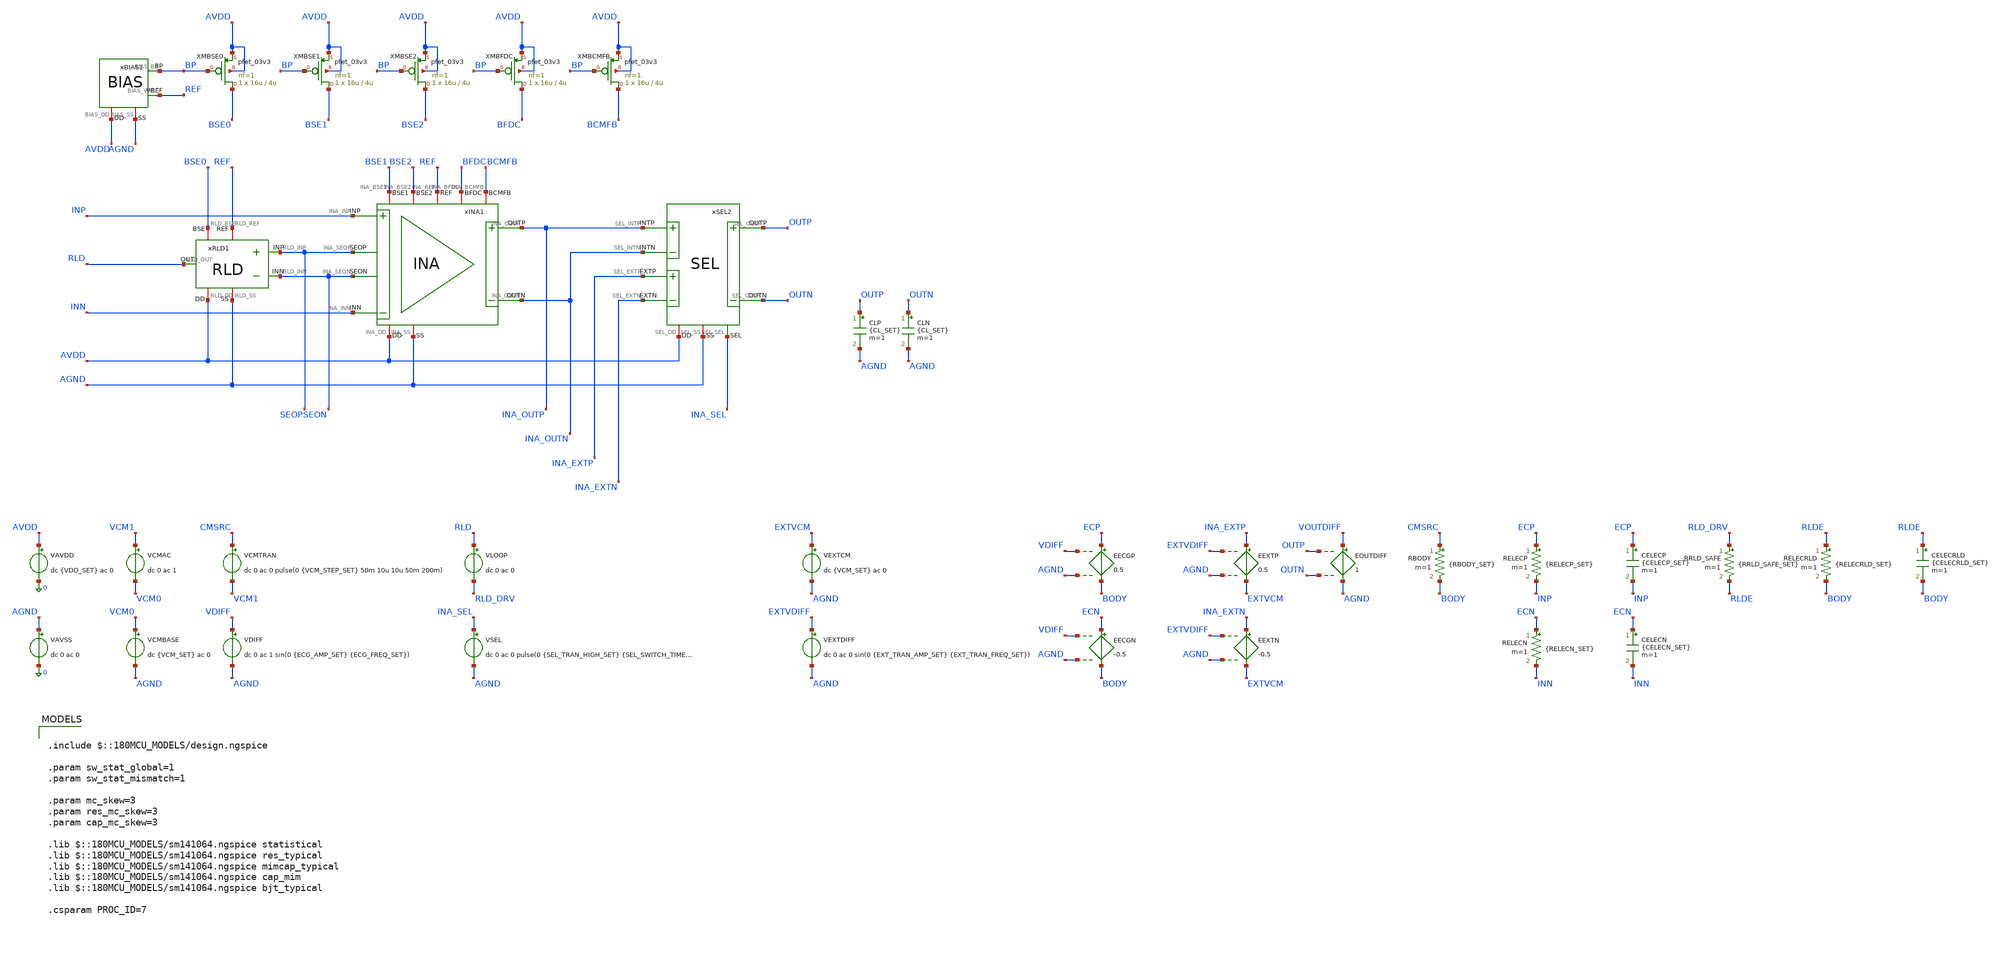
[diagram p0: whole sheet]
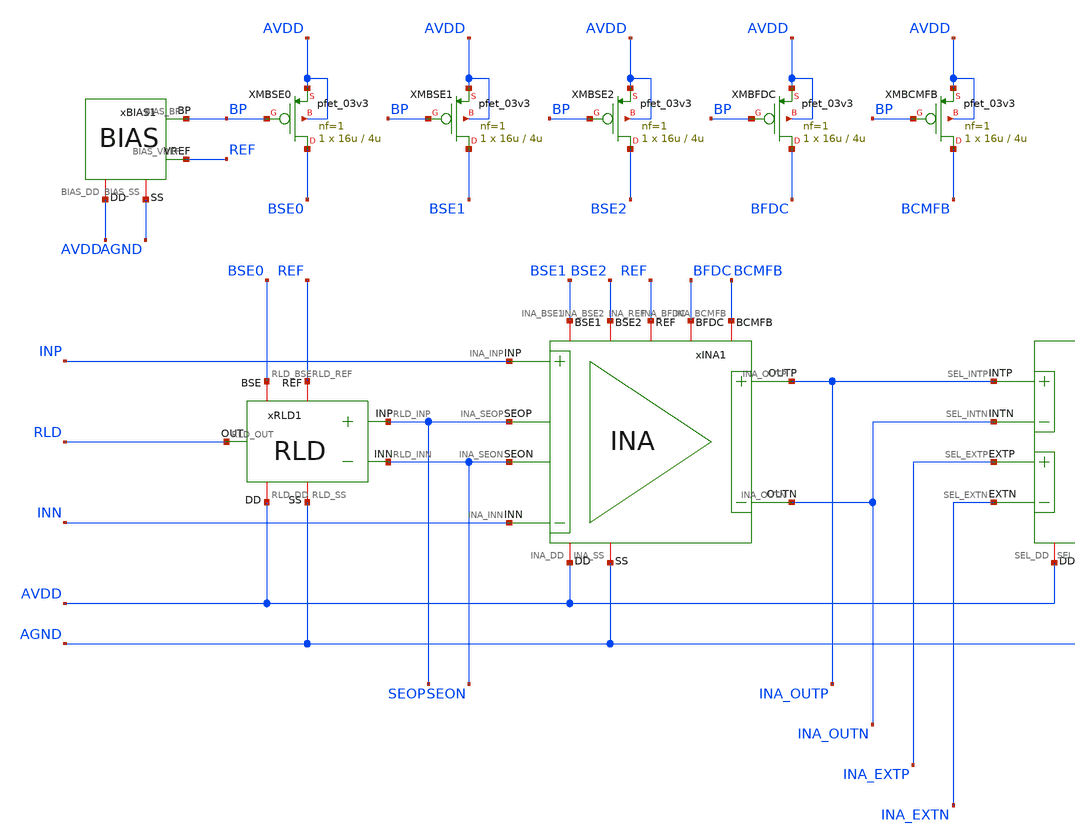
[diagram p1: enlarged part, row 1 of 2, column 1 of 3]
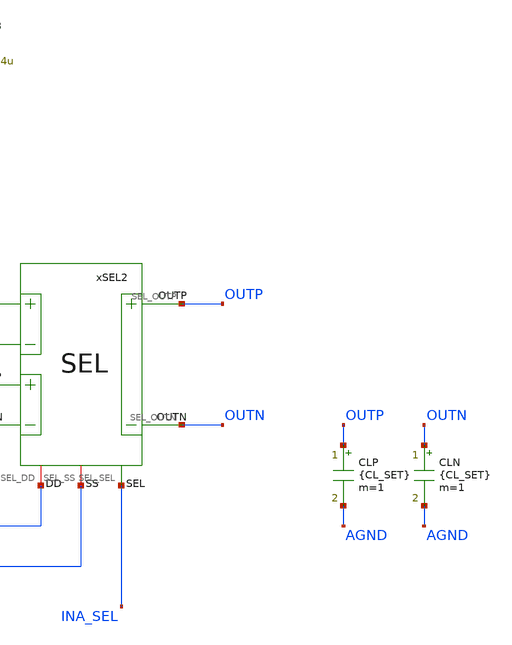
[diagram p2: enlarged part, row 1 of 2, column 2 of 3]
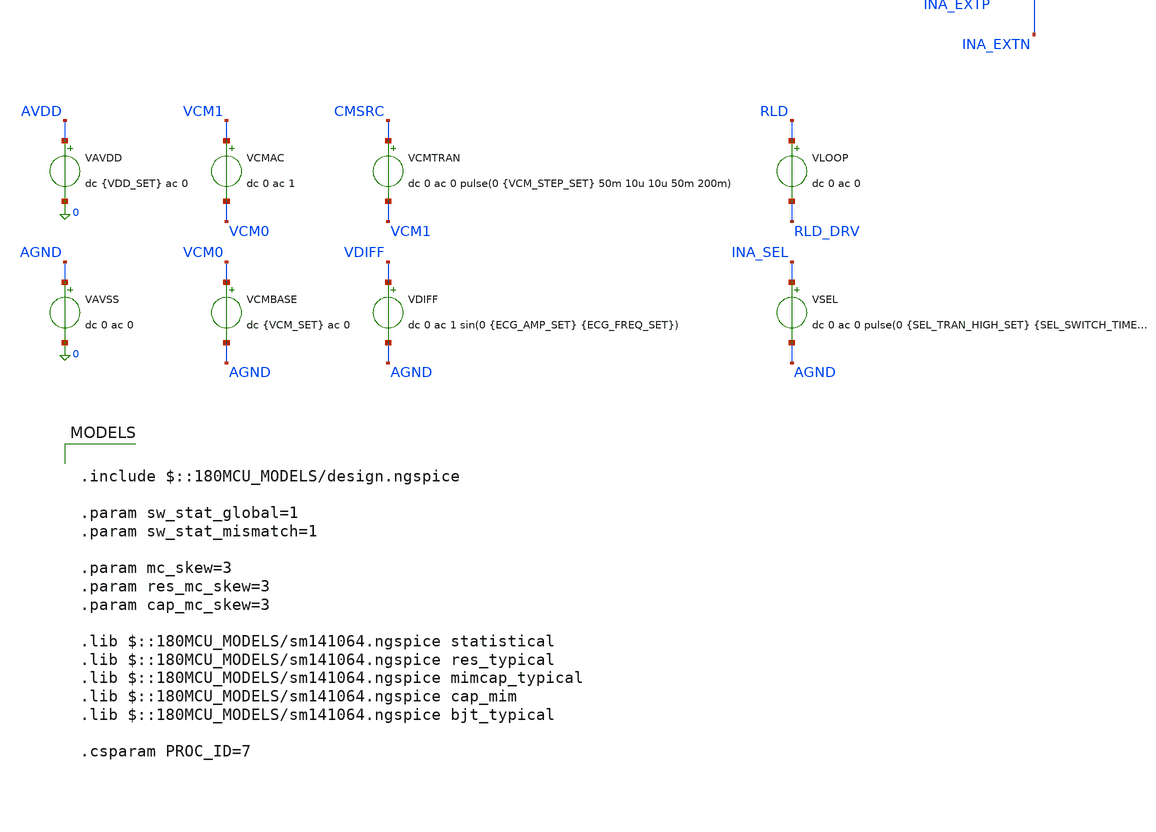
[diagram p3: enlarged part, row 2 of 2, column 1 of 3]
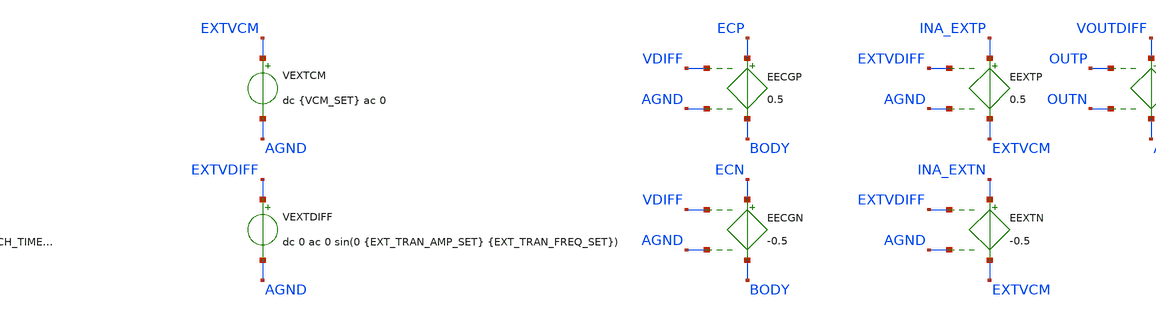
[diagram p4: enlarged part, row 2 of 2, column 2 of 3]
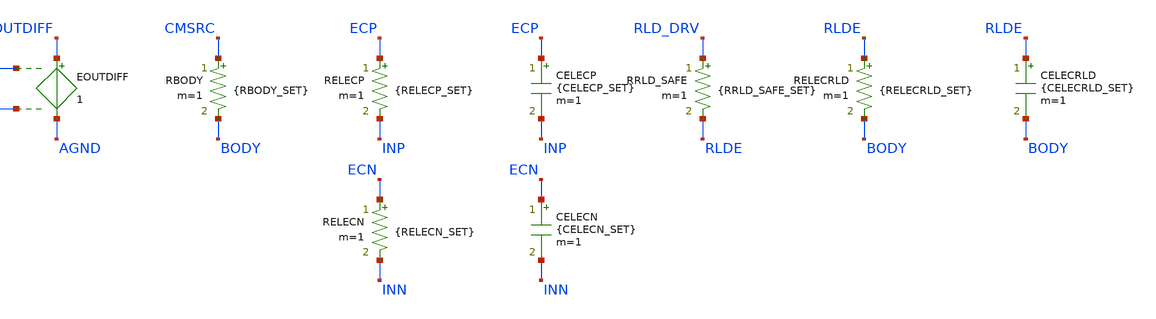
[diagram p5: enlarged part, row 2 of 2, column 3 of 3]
** sch_path: Design_Files/IC Design/Testbench/INA_RLD/INA_RLD_TB_FULL.sch
**.subckt INA_RLD_TB_FULL
xSEL2 AVDD AGND INA_OUTP INA_OUTN OUTN OUTP INA_EXTP INA_EXTN INA_SEL SEL
xINA1 AVDD AGND INP INN INA_OUTN BFDC INA_OUTP BCMFB REF SEON SEOP BSE1 BSE2 INA
xRLD1 AVDD AGND SEOP SEON RLD REF BSE0 RLD
CLP OUTP AGND {CL_SET} m=1
CLN OUTN AGND {CL_SET} m=1
xBIAS1 AVDD AGND BP REF BIAS
XMBSE0 BSE0 BP AVDD AVDD pfet_03v3 L=4u W=16u nf=1 ad='int((nf+1)/2) * W/nf * 0.18u' as='int((nf+2)/2) * W/nf * 0.18u'
+ pd='2*int((nf+1)/2) * (W/nf + 0.18u)' ps='2*int((nf+2)/2) * (W/nf + 0.18u)' nrd='0.18u / W' nrs='0.18u / W'
+ sa=0 sb=0 sd=0 m=1
XMBSE1 BSE1 BP AVDD AVDD pfet_03v3 L=4u W=16u nf=1 ad='int((nf+1)/2) * W/nf * 0.18u' as='int((nf+2)/2) * W/nf * 0.18u'
+ pd='2*int((nf+1)/2) * (W/nf + 0.18u)' ps='2*int((nf+2)/2) * (W/nf + 0.18u)' nrd='0.18u / W' nrs='0.18u / W'
+ sa=0 sb=0 sd=0 m=1
XMBSE2 BSE2 BP AVDD AVDD pfet_03v3 L=4u W=16u nf=1 ad='int((nf+1)/2) * W/nf * 0.18u' as='int((nf+2)/2) * W/nf * 0.18u'
+ pd='2*int((nf+1)/2) * (W/nf + 0.18u)' ps='2*int((nf+2)/2) * (W/nf + 0.18u)' nrd='0.18u / W' nrs='0.18u / W'
+ sa=0 sb=0 sd=0 m=1
XMBFDC BFDC BP AVDD AVDD pfet_03v3 L=4u W=16u nf=1 ad='int((nf+1)/2) * W/nf * 0.18u' as='int((nf+2)/2) * W/nf * 0.18u'
+ pd='2*int((nf+1)/2) * (W/nf + 0.18u)' ps='2*int((nf+2)/2) * (W/nf + 0.18u)' nrd='0.18u / W' nrs='0.18u / W'
+ sa=0 sb=0 sd=0 m=1
XMBCMFB BCMFB BP AVDD AVDD pfet_03v3 L=4u W=16u nf=1 ad='int((nf+1)/2) * W/nf * 0.18u' as='int((nf+2)/2) * W/nf * 0.18u'
+ pd='2*int((nf+1)/2) * (W/nf + 0.18u)' ps='2*int((nf+2)/2) * (W/nf + 0.18u)' nrd='0.18u / W' nrs='0.18u / W'
+ sa=0 sb=0 sd=0 m=1
VAVDD AVDD 0 dc {VDD_SET} ac 0
.save i(vavdd)
VCMBASE VCM0 AGND dc {VCM_SET} ac 0
VCMAC VCM1 VCM0 dc 0 ac 1
VAVSS AGND 0 dc 0 ac 0
VCMTRAN CMSRC VCM1 dc 0 ac 0 pulse(0 {VCM_STEP_SET} 50m 10u 10u 50m 200m)
EECGP ECP BODY VDIFF AGND 0.5
EECGN ECN BODY VDIFF AGND -0.5
EEXTP INA_EXTP EXTVCM EXTVDIFF AGND 0.5
VDIFF VDIFF AGND dc 0 ac 1 sin(0 {ECG_AMP_SET} {ECG_FREQ_SET})
VLOOP RLD RLD_DRV dc 0 ac 0
.save i(vloop)
VSEL INA_SEL AGND dc 0 ac 0 pulse(0 {SEL_TRAN_HIGH_SET} {SEL_SWITCH_TIME_SET} 1u 1u 400m 800m)
VEXTCM EXTVCM AGND dc {VCM_SET} ac 0
VEXTDIFF EXTVDIFF AGND dc 0 ac 0 sin(0 {EXT_TRAN_AMP_SET} {EXT_TRAN_FREQ_SET})
EEXTN INA_EXTN EXTVCM EXTVDIFF AGND -0.5
EOUTDIFF VOUTDIFF AGND OUTP OUTN 1
RBODY CMSRC BODY {RBODY_SET} m=1
RELECP ECP INP {RELECP_SET} m=1
RELECN ECN INN {RELECN_SET} m=1
CELECP ECP INP {CELECP_SET} m=1
CELECN ECN INN {CELECN_SET} m=1
RRLD_SAFE RLD_DRV RLDE {RRLD_SAFE_SET} m=1
RELECRLD RLDE BODY {RELECRLD_SET} m=1
CELECRLD RLDE BODY {CELECRLD_SET} m=1
**** begin user architecture code

.include $::180MCU_MODELS/design.ngspice

.param sw_stat_global=1
.param sw_stat_mismatch=1

.param mc_skew=3
.param res_mc_skew=3
.param cap_mc_skew=3

.lib $::180MCU_MODELS/sm141064.ngspice statistical
.lib $::180MCU_MODELS/sm141064.ngspice res_typical
.lib $::180MCU_MODELS/sm141064.ngspice mimcap_typical
.lib $::180MCU_MODELS/sm141064.ngspice cap_mim
.lib $::180MCU_MODELS/sm141064.ngspice bjt_typical

.csparam PROC_ID=7



.param VDD_SET=3.3
.param TEMP_SET=27
.param VCM_SET={VDD_SET/2}

.param CL_SET=10p

.param ECG_AMP_SET=0.5m
.param ECG_FREQ_SET=10
.param VCM_STEP_SET=300m

.param RBODY_SET=100Meg

.param RELECP_SET=100k
.param RELECN_SET=100k
.param CELECP_SET=100n
.param CELECN_SET=100n

.param RRLD_SAFE_SET=1Meg
.param RELECRLD_SET=100k
.param CELECRLD_SET=100n

.param SEL_TRAN_HIGH_SET=0
.param SEL_SWITCH_TIME_SET=200m
.param EXT_TRAN_AMP_SET=0
.param EXT_TRAN_FREQ_SET=25

.csparam MC_RUNS=200

.temp {TEMP_SET}

.options gmin=1e-12
.options rshunt=1e12
.options method=gear





.control

destroy all

set noaskquit
set wr_singlescale
unset wr_vecnames

option klu
option numdgt=15
option method=gear
option maxord=2
option plotwinsize=0


if $&PROC_ID = 5
set proc=MM
else
if $&PROC_ID = 6
set proc=GL
else
set proc=FULL
end
end


shell mkdir -p /foss/designs/ECG_Acquisition_IC/Measurement_Results/IC_Simulation/INA_RLD/{$proc}.Result_txt

shell rm -f /foss/designs/ECG_Acquisition_IC/Measurement_Results/IC_Simulation/INA_RLD/{$proc}.Result_txt/{$proc}.mc_summary.txt
shell rm -f /foss/designs/ECG_Acquisition_IC/Measurement_Results/IC_Simulation/INA_RLD/{$proc}.Result_txt/{$proc}.mc_debug_op.txt
shell rm -f /foss/designs/ECG_Acquisition_IC/Measurement_Results/IC_Simulation/INA_RLD/{$proc}.Result_txt/{$proc}.mc_bad_ac_run_*.txt


echo run vos_in_V out_cm_error_V rld_dc_error_V idd_A power_W s1_gain s2_gain ina_gain ina_gain_error_pct
+ ina_gain_150 rld_ugf_Hz rld_pm_deg cm_supp_60_dB cm_supp_150_dB > /foss/designs/ECG_Acquisition_IC/Measurement_Results/IC_Simulation/INA_RLD/{$proc}.Result_txt/{$proc}.mc_summary.txt

echo run REF_V BP_V BFDC_V BCMFB_V SEOP_V SEON_V SE_CM_V SE_DIFF_V FDINP_V FDINN_V FDIN_CM_V FDIN_DIFF_V
+ INA_OUTP_V INA_OUTN_V INA_OUT_CM_V INA_OUT_DIFF_V RLD_V IBSE1_A IBSE2_A IBFDC_A IBCMFB_A IDD_A POWER_W
+ > /foss/designs/ECG_Acquisition_IC/Measurement_Results/IC_Simulation/INA_RLD/{$proc}.Result_txt/{$proc}.mc_debug_op.txt


let run=1
let mc_runs=$&MC_RUNS


dowhile run <= mc_runs

set runnum=$&run

setseed $runnum
mc_source

option klu
option numdgt=15
option method=gear
option maxord=2
option plotwinsize=0


save all

save @m.xmbse1.m0[id]
save @m.xmbse2.m0[id]
save @m.xmbfdc.m0[id]
save @m.xmbcmfb.m0[id]


* BAL

alter RELECP 100k
alter RELECN 100k
alter CELECP 100n
alter CELECN 100n

alter RRLD_SAFE 1Meg

alter @VSEL[DC]=0
alter @VDIFF[ACMAG]=0
alter @VCMAC[ACMAG]=0
alter @VLOOP[ACMAG]=0
alter @VEXTDIFF[ACMAG]=0


* OP

op

let ref_op=v(REF)-v(AGND)
let bp_op=v(BP)-v(AGND)
let bfdc_op=v(BFDC)-v(AGND)
let bcmfb_op=v(BCMFB)-v(AGND)

let seop_op=v(SEOP)-v(AGND)
let seon_op=v(SEON)-v(AGND)
let se_cm_op=0.5*(v(SEOP)+v(SEON))-v(AGND)
let se_diff_op=v(SEOP)-v(SEON)

let fdinp_op=v(xina1.ina_fdinp)-v(AGND)
let fdinn_op=v(xina1.ina_fdinn)-v(AGND)
let fdin_cm_op=0.5*(v(xina1.ina_fdinp)+v(xina1.ina_fdinn))-v(AGND)
let fdin_diff_op=v(xina1.ina_fdinp)-v(xina1.ina_fdinn)

let ina_outp_op=v(INA_OUTP)-v(AGND)
let ina_outn_op=v(INA_OUTN)-v(AGND)
let ina_out_cm_op=0.5*(v(INA_OUTP)+v(INA_OUTN))-v(AGND)
let ina_out_diff_op=v(INA_OUTP)-v(INA_OUTN)

let ina_offset_out=ina_out_diff_op

let out_cm=0.5*(v(OUTP)+v(OUTN))-v(AGND)
let out_cm_error=out_cm-ref_op

let rld_op=v(RLD)-v(AGND)
let rld_dc_error=rld_op-ref_op

let ibse1=abs(@m.xmbse1.m0[id])
let ibse2=abs(@m.xmbse2.m0[id])
let ibfdc=abs(@m.xmbfdc.m0[id])
let ibcmfb=abs(@m.xmbcmfb.m0[id])

let idd_total=abs(vavdd#branch)
let power_total=(v(AVDD)-v(AGND))*idd_total


set ref_val=$&ref_op
set bp_val=$&bp_op
set bfdc_val=$&bfdc_op
set bcmfb_val=$&bcmfb_op

set seop_val=$&seop_op
set seon_val=$&seon_op
set se_cm_val=$&se_cm_op
set se_diff_val=$&se_diff_op

set fdinp_val=$&fdinp_op
set fdinn_val=$&fdinn_op
set fdin_cm_val=$&fdin_cm_op
set fdin_diff_val=$&fdin_diff_op

set ina_outp_val=$&ina_outp_op
set ina_outn_val=$&ina_outn_op
set ina_out_cm_val=$&ina_out_cm_op
set ina_out_diff_val=$&ina_out_diff_op

set rld_op_val=$&rld_op

set ibse1_val=$&ibse1
set ibse2_val=$&ibse2
set ibfdc_val=$&ibfdc
set ibcmfb_val=$&ibcmfb

set ina_offset_out_val=$&ina_offset_out
set out_cm_error_val=$&out_cm_error
set rld_dc_error_val=$&rld_dc_error
set idd_val=$&idd_total
set power_val=$&power_total


echo $runnum $ref_val $bp_val $bfdc_val $bcmfb_val $seop_val $seon_val $se_cm_val $se_diff_val $fdinp_val
+ $fdinn_val $fdin_cm_val $fdin_diff_val $ina_outp_val $ina_outn_val $ina_out_cm_val $ina_out_diff_val
+ $rld_op_val $ibse1_val $ibse2_val $ibfdc_val $ibcmfb_val $idd_val $power_val >> /foss/designs/ECG_Acquisition_IC/Measurement_Results/IC_Simulation/INA_RLD/{$proc}.Result_txt/{$proc}.mc_debug_op.txt


destroy all


* INA AC

alter RRLD_SAFE 1Meg

alter @VSEL[DC]=0
alter @VDIFF[ACMAG]=1
alter @VDIFF[ACPHASE]=0
alter @VCMAC[ACMAG]=0
alter @VLOOP[ACMAG]=0
alter @VEXTDIFF[ACMAG]=0

ac dec 100 0.1 1Meg

let vin_diff=v(INP)-v(INN)
let se_diff=v(SEOP)-v(SEON)
let ina_diff=v(INA_OUTP)-v(INA_OUTN)

let s1_gain=mag(se_diff/vin_diff)
let s2_gain=mag(ina_diff/se_diff)
let ina_gain=mag(ina_diff/vin_diff)

meas ac s1_gain_10 find s1_gain at=10
meas ac s2_gain_10 find s2_gain at=10
meas ac ina_gain_10 find ina_gain at=10
meas ac ina_gain_150 find ina_gain at=150

let ina_gain_error_pct=100*(ina_gain_10/240-1)
let vos_in=$ina_offset_out_val/ina_gain_10

set vos_val=$&vos_in
set s1_val=$&s1_gain_10
set s2_val=$&s2_gain_10
set ina_val=$&ina_gain_10
set ina_err_val=$&ina_gain_error_pct
set ina150_val=$&ina_gain_150


* BAD GAIN DEBUG

if $&ina_gain_error_pct < -90

let vin_diff_real=real(vin_diff)
let vin_diff_imag=imag(vin_diff)

let se_diff_real=real(se_diff)
let se_diff_imag=imag(se_diff)

let ina_diff_real=real(ina_diff)
let ina_diff_imag=imag(ina_diff)

setscale frequency

wrdata /foss/designs/ECG_Acquisition_IC/Measurement_Results/IC_Simulation/INA_RLD/{$proc}.Result_txt/{$proc}.mc_bad_ac_run_{$runnum}.txt
+ vin_diff_real vin_diff_imag se_diff_real se_diff_imag ina_diff_real ina_diff_imag

end


destroy all


* RLD LOOP

alter RRLD_SAFE 1Meg

alter @VSEL[DC]=0
alter @VDIFF[ACMAG]=0
alter @VCMAC[ACMAG]=0
alter @VLOOP[ACMAG]=1
alter @VLOOP[ACPHASE]=0
alter @VEXTDIFF[ACMAG]=0

ac dec 100 0.1 100k

let loop_in=v(RLD_DRV)-v(AGND)
let loop_out=v(RLD)-v(AGND)

let loop_tf=-loop_out/loop_in
let loop_mag=mag(loop_tf)
let loop_phase=(180/3.141592653589793)*cph(loop_tf)

meas ac rld_ugf when loop_mag=1 cross=1
meas ac rld_phase find loop_phase at=$&rld_ugf

let rld_pm=180+rld_phase

set ugf_val=$&rld_ugf
set pm_val=$&rld_pm

destroy all


* CM OFF

alter RRLD_SAFE 1e15

alter @VSEL[DC]=0
alter @VDIFF[ACMAG]=0
alter @VCMAC[ACMAG]=1
alter @VCMAC[ACPHASE]=0
alter @VLOOP[ACMAG]=0
alter @VEXTDIFF[ACMAG]=0

ac dec 100 1 1k

let vin_cm=0.5*(v(INP)+v(INN))-v(AGND)
let vin_cm_mag=mag(vin_cm)

meas ac vin_cm_off_60 find vin_cm_mag at=60
meas ac vin_cm_off_150 find vin_cm_mag at=150

set vin_cm_off_60_val=$&vin_cm_off_60
set vin_cm_off_150_val=$&vin_cm_off_150

destroy all


* CM ON

alter RRLD_SAFE 1Meg

alter @VSEL[DC]=0
alter @VDIFF[ACMAG]=0
alter @VCMAC[ACMAG]=1
alter @VCMAC[ACPHASE]=0
alter @VLOOP[ACMAG]=0
alter @VEXTDIFF[ACMAG]=0

ac dec 100 1 1k

let vin_cm=0.5*(v(INP)+v(INN))-v(AGND)
let vin_cm_mag=mag(vin_cm)

meas ac vin_cm_on_60 find vin_cm_mag at=60
meas ac vin_cm_on_150 find vin_cm_mag at=150

let cm_supp_60=20*log10($vin_cm_off_60_val/vin_cm_on_60)
let cm_supp_150=20*log10($vin_cm_off_150_val/vin_cm_on_150)

set cm_supp_60_val=$&cm_supp_60
set cm_supp_150_val=$&cm_supp_150


* SUMMARY

echo $runnum $vos_val $out_cm_error_val $rld_dc_error_val $idd_val $power_val $s1_val $s2_val $ina_val
+ $ina_err_val $ina150_val $ugf_val $pm_val $cm_supp_60_val $cm_supp_150_val >> /foss/designs/ECG_Acquisition_IC/Measurement_Results/IC_Simulation/INA_RLD/{$proc}.Result_txt/{$proc}.mc_summary.txt


destroy all

let run=run+1

end


quit

.endc


**** end user architecture code
**.ends
.end
